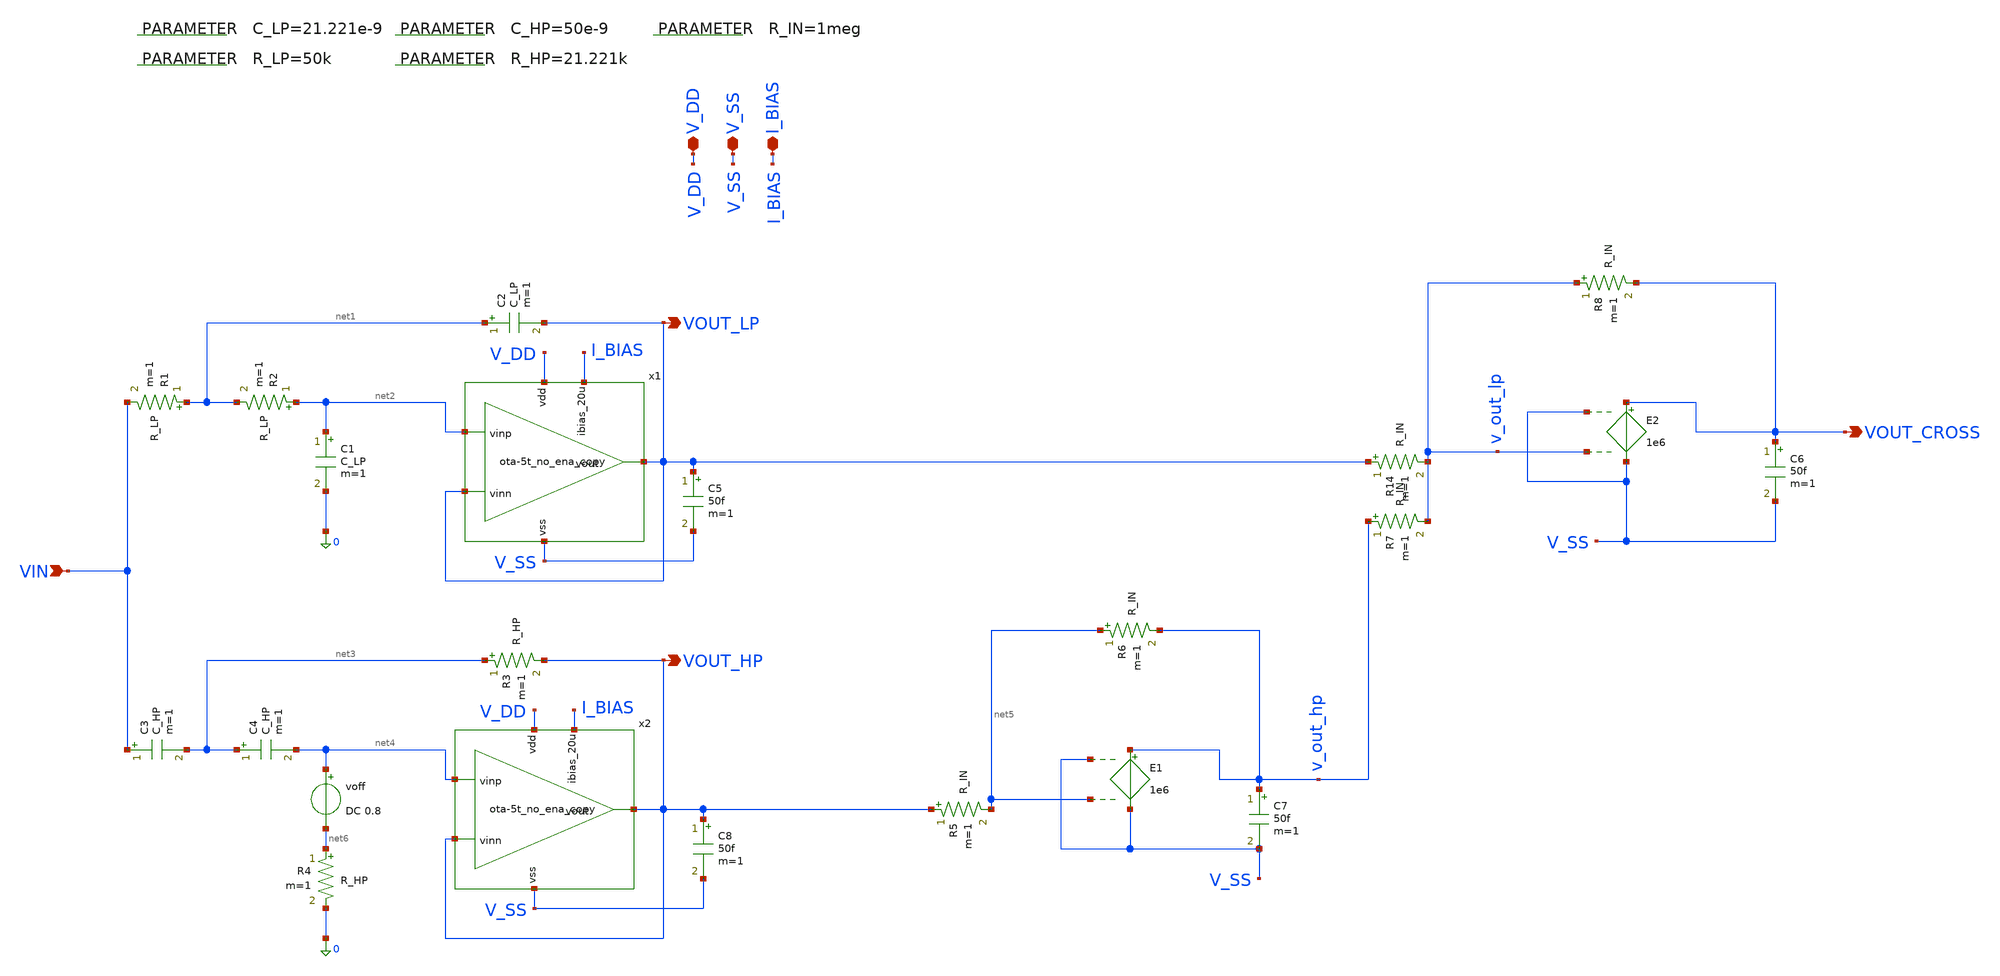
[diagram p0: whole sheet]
** sch_path: 004_Real_Circuits/002_version_no_enable/linkwtz_riley_crossover_pretl_OTA.sch
**.subckt linkwtz_riley_crossover_pretl_OTA VOUT_LP VIN V_DD VOUT_HP V_SS I_BIAS VOUT_CROSS
*.opin VOUT_LP
*.ipin VIN
*.iopin V_DD
*.opin VOUT_HP
*.iopin V_SS
*.iopin I_BIAS
*.opin VOUT_CROSS
R1 net1 VIN R_LP m=1
.param R_IN=1meg
R2 net2 net1 R_LP m=1
C1 net2 0 C_LP m=1
C2 net1 VOUT_LP C_LP m=1
C3 VIN net3 C_HP m=1
C4 net3 net4 C_HP m=1
R3 net3 VOUT_HP R_HP m=1
R4 net6 0 R_HP m=1
R5 VOUT_HP net5 R_IN m=1
R6 net5 v_out_hp R_IN m=1
R14 VOUT_LP v_out_lp R_IN m=1
R7 v_out_hp v_out_lp R_IN m=1
R8 v_out_lp VOUT_CROSS R_IN m=1
.param C_LP=21.221e-9
.param R_LP=50k
.param C_HP=50e-9
.param R_HP=21.221k
C5 VOUT_LP V_SS 50f m=1
C6 VOUT_CROSS V_SS 50f m=1
C7 v_out_hp V_SS 50f m=1
C8 VOUT_HP V_SS 50f m=1
voff net4 net6 DC 0.8
E1 v_out_hp V_SS V_SS net5 1e6
E2 VOUT_CROSS V_SS V_SS v_out_lp 1e6
x1 V_DD VOUT_LP net2 VOUT_LP I_BIAS V_SS ota-5t_no_ena_copy
x2 V_DD VOUT_HP net4 VOUT_HP I_BIAS V_SS ota-5t_no_ena_copy
**.ends
.end
